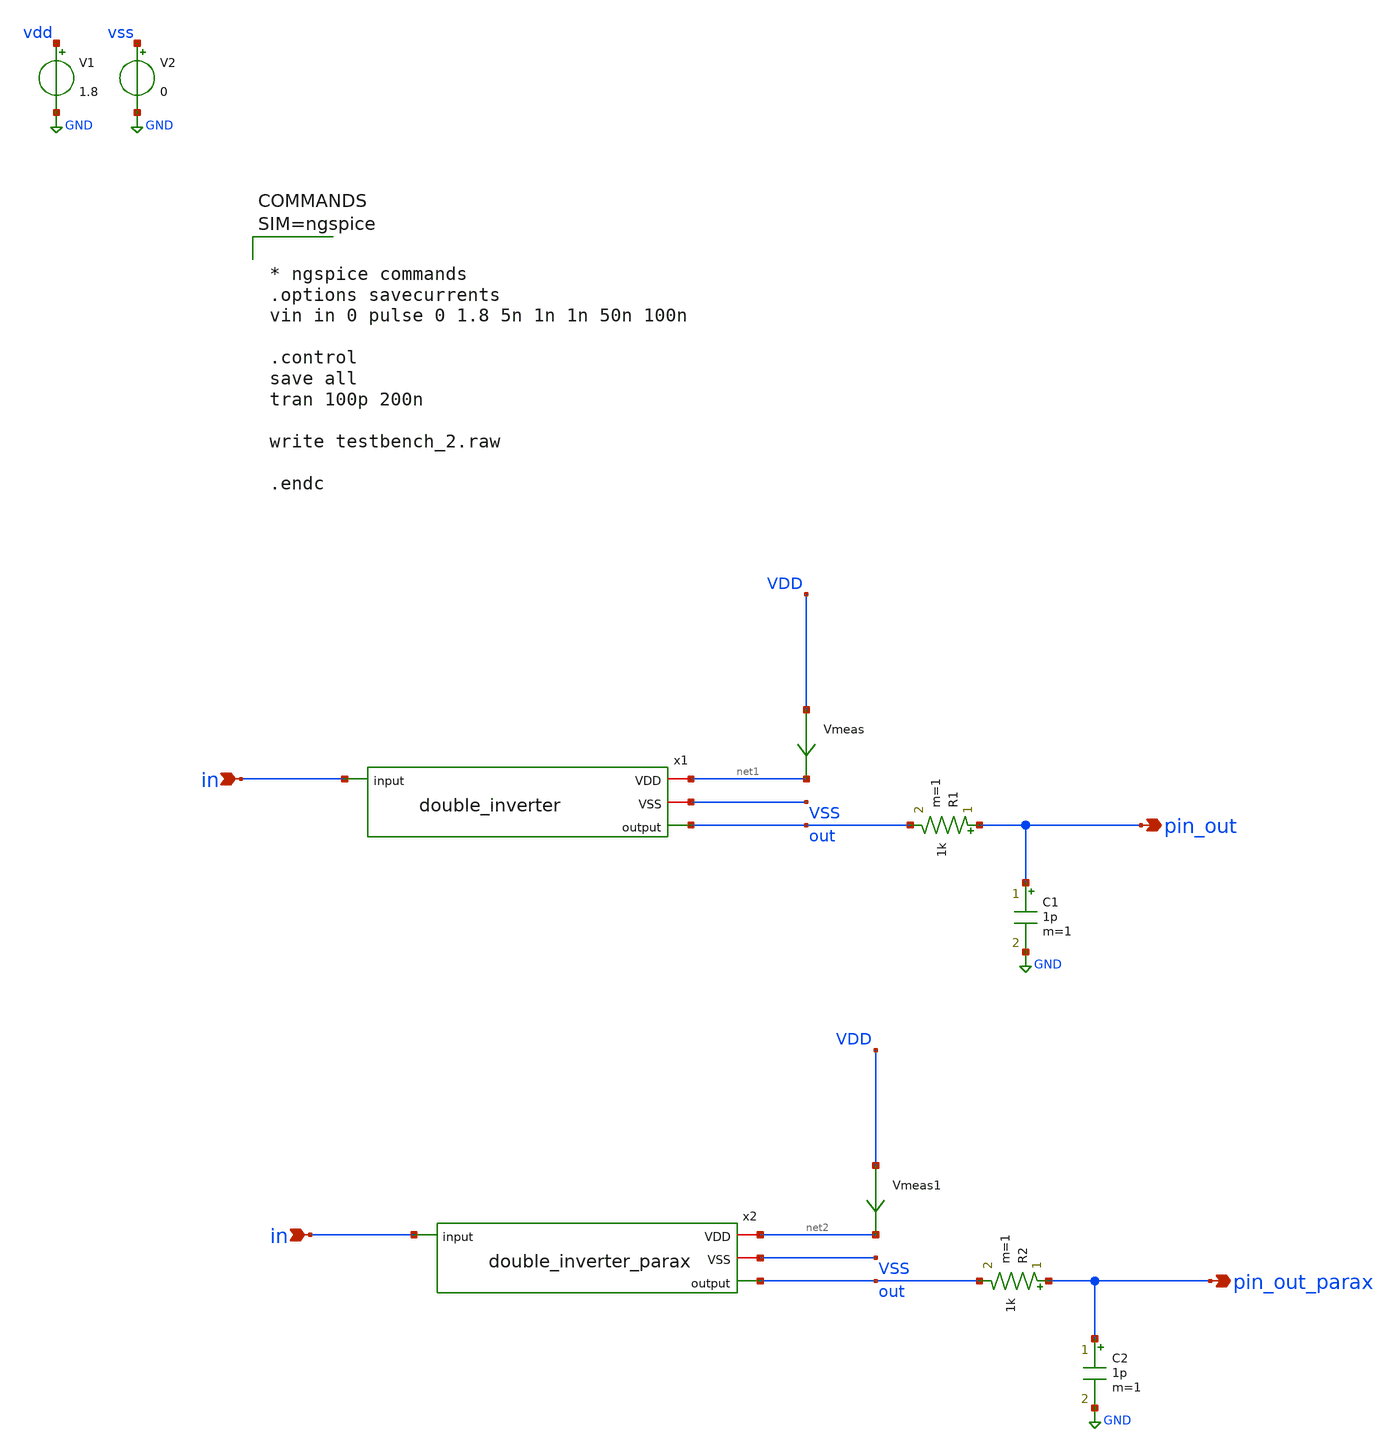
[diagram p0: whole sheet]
** sch_path: xschem/testbench_2.sch
**.subckt testbench_2 in in pin_out pin_out_parax
*.ipin in
*.ipin in
*.opin pin_out
*.opin pin_out_parax
V1 vdd GND 1.8
V2 vss GND 0
x1 net1 VSS in out double_inverter
R1 pin_out out 1k m=1
C1 pin_out GND 1p m=1
Vmeas VDD net1 0
.save i(vmeas)
x2 net2 VSS in out double_inverter_parax
R2 pin_out_parax out 1k m=1
C2 pin_out_parax GND 1p m=1
Vmeas1 VDD net2 0
.save i(vmeas1)
**** begin user architecture code

** opencircuitdesign pdks install
.lib $::SKYWATER_MODELS/sky130.lib.spice tt





* ngspice commands
.options savecurrents
vin in 0 pulse 0 1.8 5n 1n 1n 50n 100n

.control
save all
tran 100p 200n

write testbench_2.raw

.endc





**** end user architecture code
**.ends

* expanding   symbol:  double_inverter.sym # of pins=4
** sym_path: xschem/double_inverter.sym
** sch_path: xschem/double_inverter.sch
.subckt double_inverter VDD VSS input output
*.iopin VDD
*.iopin VSS
*.ipin input
*.opin output
XM1 inverted input VDD VDD sky130_fd_pr__pfet_01v8 L=0.15 W=1 nf=1 ad='int((nf+1)/2) * W/nf * 0.29' as='int((nf+2)/2) * W/nf * 0.29'
+ pd='2*int((nf+1)/2) * (W/nf + 0.29)' ps='2*int((nf+2)/2) * (W/nf + 0.29)' nrd='0.29 / W' nrs='0.29 / W'
+ sa=0 sb=0 sd=0 mult=1 m=1
XM2 inverted input VSS VSS sky130_fd_pr__nfet_01v8 L=0.15 W=1 nf=1 ad='int((nf+1)/2) * W/nf * 0.29' as='int((nf+2)/2) * W/nf * 0.29'
+ pd='2*int((nf+1)/2) * (W/nf + 0.29)' ps='2*int((nf+2)/2) * (W/nf + 0.29)' nrd='0.29 / W' nrs='0.29 / W'
+ sa=0 sb=0 sd=0 mult=1 m=1
XM3 output inverted VDD VDD sky130_fd_pr__pfet_01v8 L=0.15 W=20 nf=20 ad='int((nf+1)/2) * W/nf * 0.29'
+ as='int((nf+2)/2) * W/nf * 0.29' pd='2*int((nf+1)/2) * (W/nf + 0.29)' ps='2*int((nf+2)/2) * (W/nf + 0.29)'
+ nrd='0.29 / W' nrs='0.29 / W' sa=0 sb=0 sd=0 mult=1 m=1
XM4 output inverted VSS VSS sky130_fd_pr__nfet_01v8 L=0.15 W=20 nf=20 ad='int((nf+1)/2) * W/nf * 0.29'
+ as='int((nf+2)/2) * W/nf * 0.29' pd='2*int((nf+1)/2) * (W/nf + 0.29)' ps='2*int((nf+2)/2) * (W/nf + 0.29)'
+ nrd='0.29 / W' nrs='0.29 / W' sa=0 sb=0 sd=0 mult=1 m=1
.ends


* expanding   symbol:  double_inverter_parax.sym # of pins=4
** sym_path: xschem/double_inverter.sym
.include [file normalize ../mag/double_inverter.sim.spice]
.GLOBAL GND
.end
